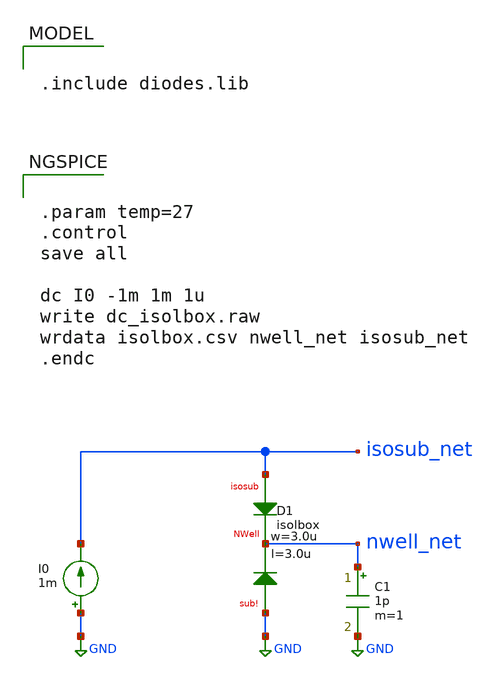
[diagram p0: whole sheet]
** sch_path: ihp-sg13g2/libs.tech/xschem/sg13g2_tests/dc_isolbox.sch
* Copyright 2023 IHP PDK Authors
**.subckt dc_isolbox
I0 GND isosub_net 1m
C1 nwell_net GND 1p m=1
XD1 isosub_net nwell_net GND isolbox l=3.0u w=3.0u
**** begin user architecture code

.include diodes.lib



.param temp=27
.control
save all

dc I0 -1m 1m 1u
write dc_isolbox.raw
wrdata isolbox.csv nwell_net isosub_net
.endc


**** end user architecture code
**.ends
.GLOBAL GND
.end
